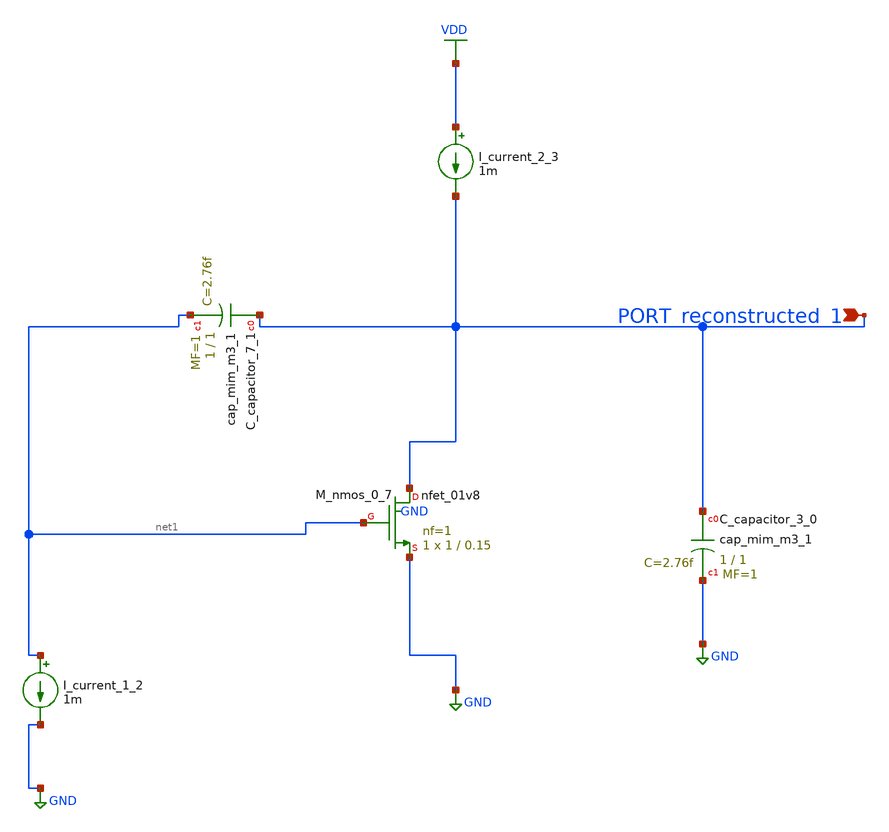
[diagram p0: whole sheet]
** sch_path: schematics/AMSNet/733.sch
**.subckt 733 PORT_reconstructed_1
*.ipin PORT_reconstructed_1
XC_capacitor_3_0 PORT_reconstructed_1 GND sky130_fd_pr__cap_mim_m3_1 W=1 L=1 MF=1 m=1
XC_capacitor_7_1 PORT_reconstructed_1 net1 sky130_fd_pr__cap_mim_m3_1 W=1 L=1 MF=1 m=1
I_current_1_2 net1 GND 1m
I_current_2_3 VDD PORT_reconstructed_1 1m
XM_nmos_0_7 PORT_reconstructed_1 net1 GND GND sky130_fd_pr__nfet_01v8 L=0.15 W=1 nf=1 ad='int((1 + 1)/2) * 1 / 1 * 0.29'
+ as='int((1 + 2)/2) * 1 / 1 * 0.29' pd='2*int((1 + 1)/2) * (1 / 1 + 0.29)' ps='2*int((1 + 2)/2) * (1 / 1 + 0.29)'
+ nrd='0.29 / 1 ' nrs='0.29 / 1 ' sa=0 sb=0 sd=0 mult=1 m=1
**.ends
.GLOBAL GND
.GLOBAL VDD
.end
